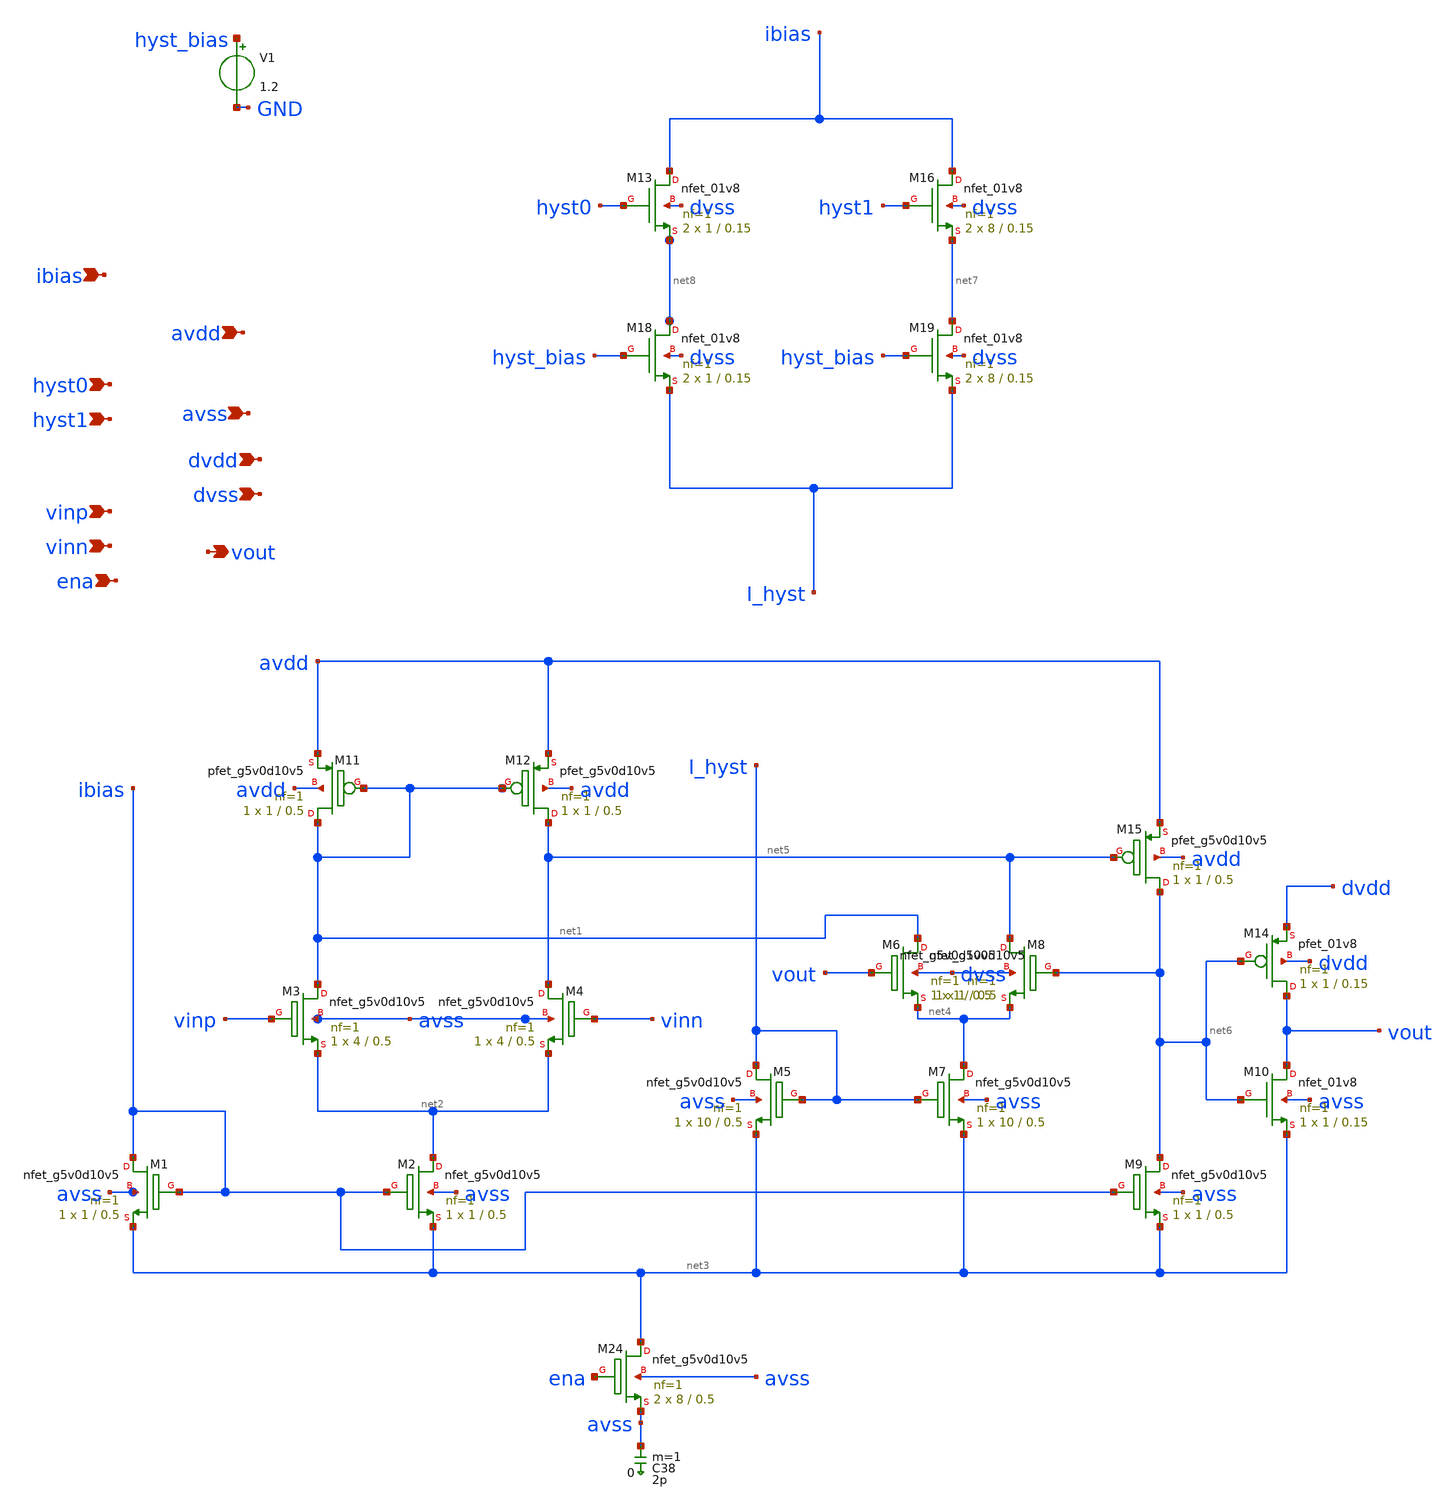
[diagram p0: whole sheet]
** sch_path: Chipalooza_April2024_Comparator/xschem/Chipalooza_April2024_Comparator (copy 1).sch
**.subckt Chipalooza_April2024_Comparator (copy 1) vinp vinn hyst0 hyst1 avdd avss dvdd dvss vout
*+ ena ibias
*.ipin vinp
*.ipin vinn
*.ipin hyst0
*.ipin hyst1
*.ipin avdd
*.ipin avss
*.ipin dvdd
*.ipin dvss
*.opin vout
*.ipin ena
*.ipin ibias
XM1 ibias ibias net3 avss sky130_fd_pr__nfet_g5v0d10v5 L=0.5 W=1 nf=1 ad='int((nf+1)/2) * W/nf * 0.29'
+ as='int((nf+2)/2) * W/nf * 0.29' pd='2*int((nf+1)/2) * (W/nf + 0.29)' ps='2*int((nf+2)/2) * (W/nf + 0.29)'
+ nrd='0.29 / W' nrs='0.29 / W' sa=0 sb=0 sd=0 mult=1 m=1
XM2 net2 ibias net3 avss sky130_fd_pr__nfet_g5v0d10v5 L=0.5 W=1 nf=1 ad='int((nf+1)/2) * W/nf * 0.29'
+ as='int((nf+2)/2) * W/nf * 0.29' pd='2*int((nf+1)/2) * (W/nf + 0.29)' ps='2*int((nf+2)/2) * (W/nf + 0.29)'
+ nrd='0.29 / W' nrs='0.29 / W' sa=0 sb=0 sd=0 mult=1 m=1
XM3 net1 vinp net2 avss sky130_fd_pr__nfet_g5v0d10v5 L=0.5 W=4 nf=1 ad='int((nf+1)/2) * W/nf * 0.29'
+ as='int((nf+2)/2) * W/nf * 0.29' pd='2*int((nf+1)/2) * (W/nf + 0.29)' ps='2*int((nf+2)/2) * (W/nf + 0.29)'
+ nrd='0.29 / W' nrs='0.29 / W' sa=0 sb=0 sd=0 mult=1 m=1
XM4 net5 vinn net2 avss sky130_fd_pr__nfet_g5v0d10v5 L=0.5 W=4 nf=1 ad='int((nf+1)/2) * W/nf * 0.29'
+ as='int((nf+2)/2) * W/nf * 0.29' pd='2*int((nf+1)/2) * (W/nf + 0.29)' ps='2*int((nf+2)/2) * (W/nf + 0.29)'
+ nrd='0.29 / W' nrs='0.29 / W' sa=0 sb=0 sd=0 mult=1 m=1
XM5 I_hyst I_hyst net3 avss sky130_fd_pr__nfet_g5v0d10v5 L=0.5 W=10 nf=1 ad='int((nf+1)/2) * W/nf * 0.29'
+ as='int((nf+2)/2) * W/nf * 0.29' pd='2*int((nf+1)/2) * (W/nf + 0.29)' ps='2*int((nf+2)/2) * (W/nf + 0.29)'
+ nrd='0.29 / W' nrs='0.29 / W' sa=0 sb=0 sd=0 mult=1 m=1
XM6 net1 vout net4 dvss sky130_fd_pr__nfet_g5v0d10v5 L=0.5 W=1 nf=1 ad='int((nf+1)/2) * W/nf * 0.29'
+ as='int((nf+2)/2) * W/nf * 0.29' pd='2*int((nf+1)/2) * (W/nf + 0.29)' ps='2*int((nf+2)/2) * (W/nf + 0.29)'
+ nrd='0.29 / W' nrs='0.29 / W' sa=0 sb=0 sd=0 mult=1 m=1
XM7 net4 I_hyst net3 avss sky130_fd_pr__nfet_g5v0d10v5 L=0.5 W=10 nf=1 ad='int((nf+1)/2) * W/nf * 0.29'
+ as='int((nf+2)/2) * W/nf * 0.29' pd='2*int((nf+1)/2) * (W/nf + 0.29)' ps='2*int((nf+2)/2) * (W/nf + 0.29)'
+ nrd='0.29 / W' nrs='0.29 / W' sa=0 sb=0 sd=0 mult=1 m=1
XM8 net5 net6 net4 dvss sky130_fd_pr__nfet_g5v0d10v5 L=0.5 W=1 nf=1 ad='int((nf+1)/2) * W/nf * 0.29'
+ as='int((nf+2)/2) * W/nf * 0.29' pd='2*int((nf+1)/2) * (W/nf + 0.29)' ps='2*int((nf+2)/2) * (W/nf + 0.29)'
+ nrd='0.29 / W' nrs='0.29 / W' sa=0 sb=0 sd=0 mult=1 m=1
XM9 net6 ibias net3 avss sky130_fd_pr__nfet_g5v0d10v5 L=0.5 W=1 nf=1 ad='int((nf+1)/2) * W/nf * 0.29'
+ as='int((nf+2)/2) * W/nf * 0.29' pd='2*int((nf+1)/2) * (W/nf + 0.29)' ps='2*int((nf+2)/2) * (W/nf + 0.29)'
+ nrd='0.29 / W' nrs='0.29 / W' sa=0 sb=0 sd=0 mult=1 m=1
XM11 net1 net1 avdd avdd sky130_fd_pr__pfet_g5v0d10v5 L=0.5 W=1 nf=1 ad='int((nf+1)/2) * W/nf * 0.29'
+ as='int((nf+2)/2) * W/nf * 0.29' pd='2*int((nf+1)/2) * (W/nf + 0.29)' ps='2*int((nf+2)/2) * (W/nf + 0.29)'
+ nrd='0.29 / W' nrs='0.29 / W' sa=0 sb=0 sd=0 mult=1 m=1
XM12 net5 net1 avdd avdd sky130_fd_pr__pfet_g5v0d10v5 L=0.5 W=1 nf=1 ad='int((nf+1)/2) * W/nf * 0.29'
+ as='int((nf+2)/2) * W/nf * 0.29' pd='2*int((nf+1)/2) * (W/nf + 0.29)' ps='2*int((nf+2)/2) * (W/nf + 0.29)'
+ nrd='0.29 / W' nrs='0.29 / W' sa=0 sb=0 sd=0 mult=1 m=1
XM15 net6 net5 avdd avdd sky130_fd_pr__pfet_g5v0d10v5 L=0.5 W=1 nf=1 ad='int((nf+1)/2) * W/nf * 0.29'
+ as='int((nf+2)/2) * W/nf * 0.29' pd='2*int((nf+1)/2) * (W/nf + 0.29)' ps='2*int((nf+2)/2) * (W/nf + 0.29)'
+ nrd='0.29 / W' nrs='0.29 / W' sa=0 sb=0 sd=0 mult=1 m=1
XM13 ibias hyst0 net8 dvss sky130_fd_pr__nfet_01v8 L=0.15 W=1 nf=1 ad='int((1 + 1)/2) * 1 / 1 * 0.29'
+ as='int((1 + 2)/2) * 1 / 1 * 0.29' pd='2*int((1 + 1)/2) * (1 / 1 + 0.29)' ps='2*int((1 + 2)/2) * (1 / 1 + 0.29)'
+ nrd='0.29 / 1 ' nrs='0.29 / 1 ' sa=0 sb=0 sd=0 mult=2 m=2
C38 avss 0 2p m=1
XM24 net3 ena avss avss sky130_fd_pr__nfet_g5v0d10v5 L=0.5 W=8 nf=1 ad='int((nf+1)/2) * W/nf * 0.29'
+ as='int((nf+2)/2) * W/nf * 0.29' pd='2*int((nf+1)/2) * (W/nf + 0.29)' ps='2*int((nf+2)/2) * (W/nf + 0.29)'
+ nrd='0.29 / W' nrs='0.29 / W' sa=0 sb=0 sd=0 mult=2 m=2
XM16 ibias hyst1 net7 dvss sky130_fd_pr__nfet_01v8 L=0.15 W=8 nf=1 ad='int((1 + 1)/2) * 8 / 1 * 0.29'
+ as='int((1 + 2)/2) * 8 / 1 * 0.29' pd='2*int((1 + 1)/2) * (8 / 1 + 0.29)' ps='2*int((1 + 2)/2) * (8 / 1 + 0.29)'
+ nrd='0.29 / 8 ' nrs='0.29 / 8 ' sa=0 sb=0 sd=0 mult=2 m=2
XM19 net7 hyst_bias I_hyst dvss sky130_fd_pr__nfet_01v8 L=0.15 W=8 nf=1 ad='int((1 + 1)/2) * 8 / 1 * 0.29'
+ as='int((1 + 2)/2) * 8 / 1 * 0.29' pd='2*int((1 + 1)/2) * (8 / 1 + 0.29)' ps='2*int((1 + 2)/2) * (8 / 1 + 0.29)'
+ nrd='0.29 / 8 ' nrs='0.29 / 8 ' sa=0 sb=0 sd=0 mult=2 m=2
XM18 net8 hyst_bias I_hyst dvss sky130_fd_pr__nfet_01v8 L=0.15 W=1 nf=1 ad='int((1 + 1)/2) * 1 / 1 * 0.29'
+ as='int((1 + 2)/2) * 1 / 1 * 0.29' pd='2*int((1 + 1)/2) * (1 / 1 + 0.29)' ps='2*int((1 + 2)/2) * (1 / 1 + 0.29)'
+ nrd='0.29 / 1 ' nrs='0.29 / 1 ' sa=0 sb=0 sd=0 mult=2 m=2
XM10 vout net6 net3 avss sky130_fd_pr__nfet_01v8 L=0.15 W=1 nf=1 ad='int((1 + 1)/2) * 1 / 1 * 0.29' as='int((1 + 2)/2) * 1 / 1 * 0.29'
+ pd='2*int((1 + 1)/2) * (1 / 1 + 0.29)' ps='2*int((1 + 2)/2) * (1 / 1 + 0.29)' nrd='0.29 / 1 ' nrs='0.29 / 1 '
+ sa=0 sb=0 sd=0 mult=1 m=1
XM14 vout net6 dvdd dvdd sky130_fd_pr__pfet_01v8 L=0.15 W=1 nf=1 ad='int((nf+1)/2) * W/nf * 0.29' as='int((nf+2)/2) * W/nf * 0.29'
+ pd='2*int((nf+1)/2) * (W/nf + 0.29)' ps='2*int((nf+2)/2) * (W/nf + 0.29)' nrd='0.29 / W' nrs='0.29 / W'
+ sa=0 sb=0 sd=0 mult=1 m=1
V1 hyst_bias GND 1.2
**.ends
.end
